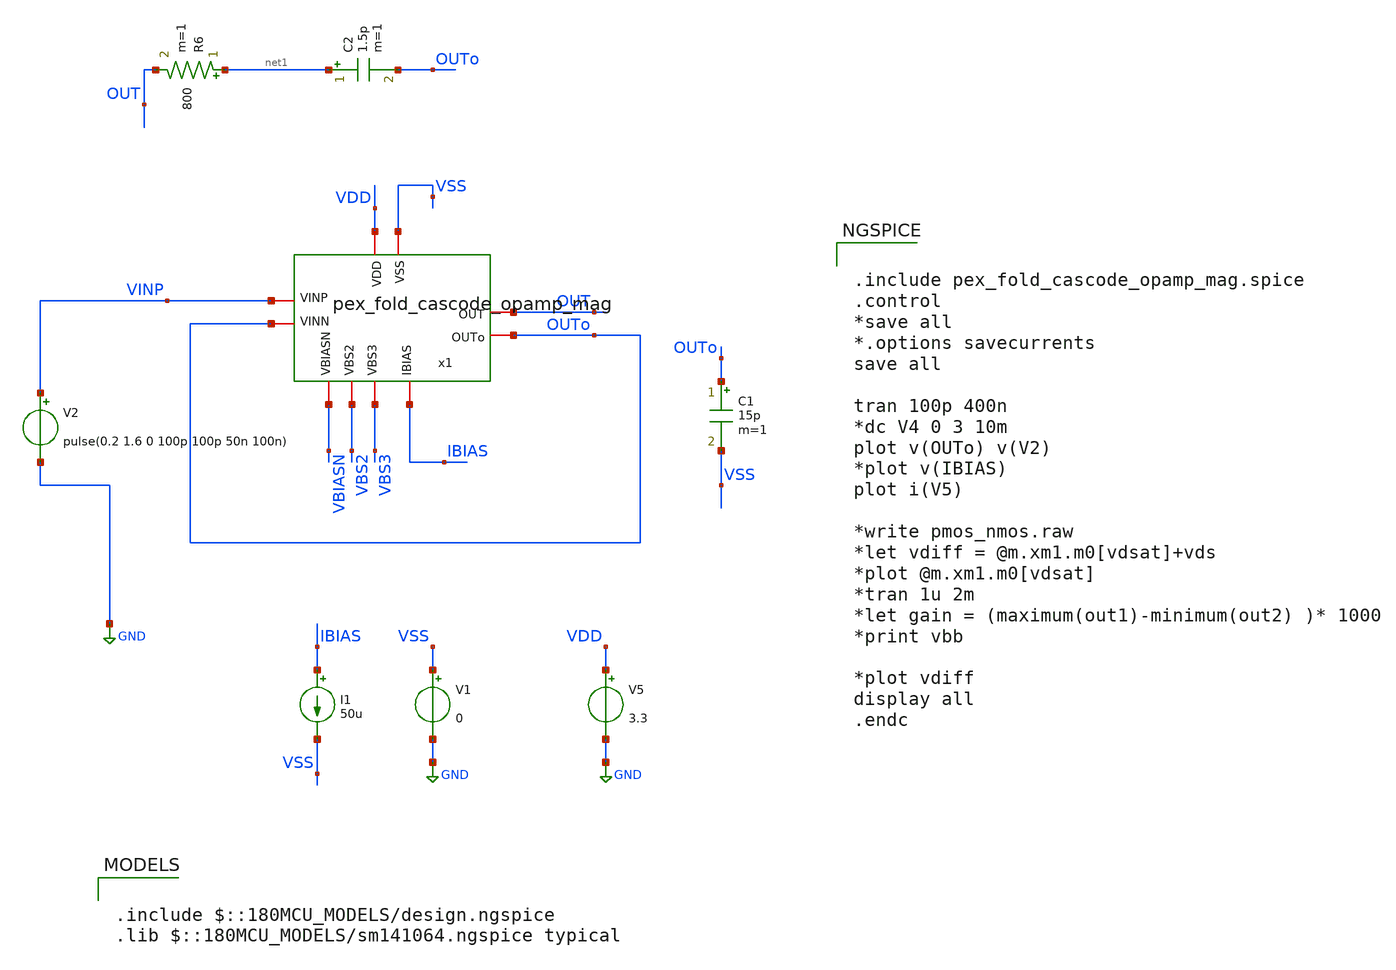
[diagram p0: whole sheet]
** sch_path: SCOP_INPUT_AND_MUX_PAKISTAN_03/Xschem/Folded_single/untitled-1.sch
**.subckt untitled-1
V5 VDD GND 3.3
V2 VINP GND pulse(0.2 1.6 0 100p 100p 50n 100n)
V1 VSS GND 0
I1 IBIAS VSS 50u
C1 OUTo VSS 15p m=1
R6 net1 OUT 800 m=1
C2 net1 OUTo 1.5p m=1
x1 OUT VDD VSS OUTo VINP IBIAS VBS2 VBS3 VBIASN OUTo pex_fold_cascode_opamp_mag
**** begin user architecture code

.include $::180MCU_MODELS/design.ngspice
.lib $::180MCU_MODELS/sm141064.ngspice typical



.include pex_fold_cascode_opamp_mag.spice
.control
*save all
*.options savecurrents
save all

tran 100p 400n
*dc V4 0 3 10m
plot v(OUTo) v(V2)
*plot v(IBIAS)
plot i(V5)

*write pmos_nmos.raw
*let vdiff = @m.xm1.m0[vdsat]+vds
*plot @m.xm1.m0[vdsat]
*tran 1u 2m
*let gain = (maximum(out1)-minimum(out2) )* 1000
*print vbb

*plot vdiff
display all
.endc


**** end user architecture code
**.ends
.GLOBAL GND
.end
